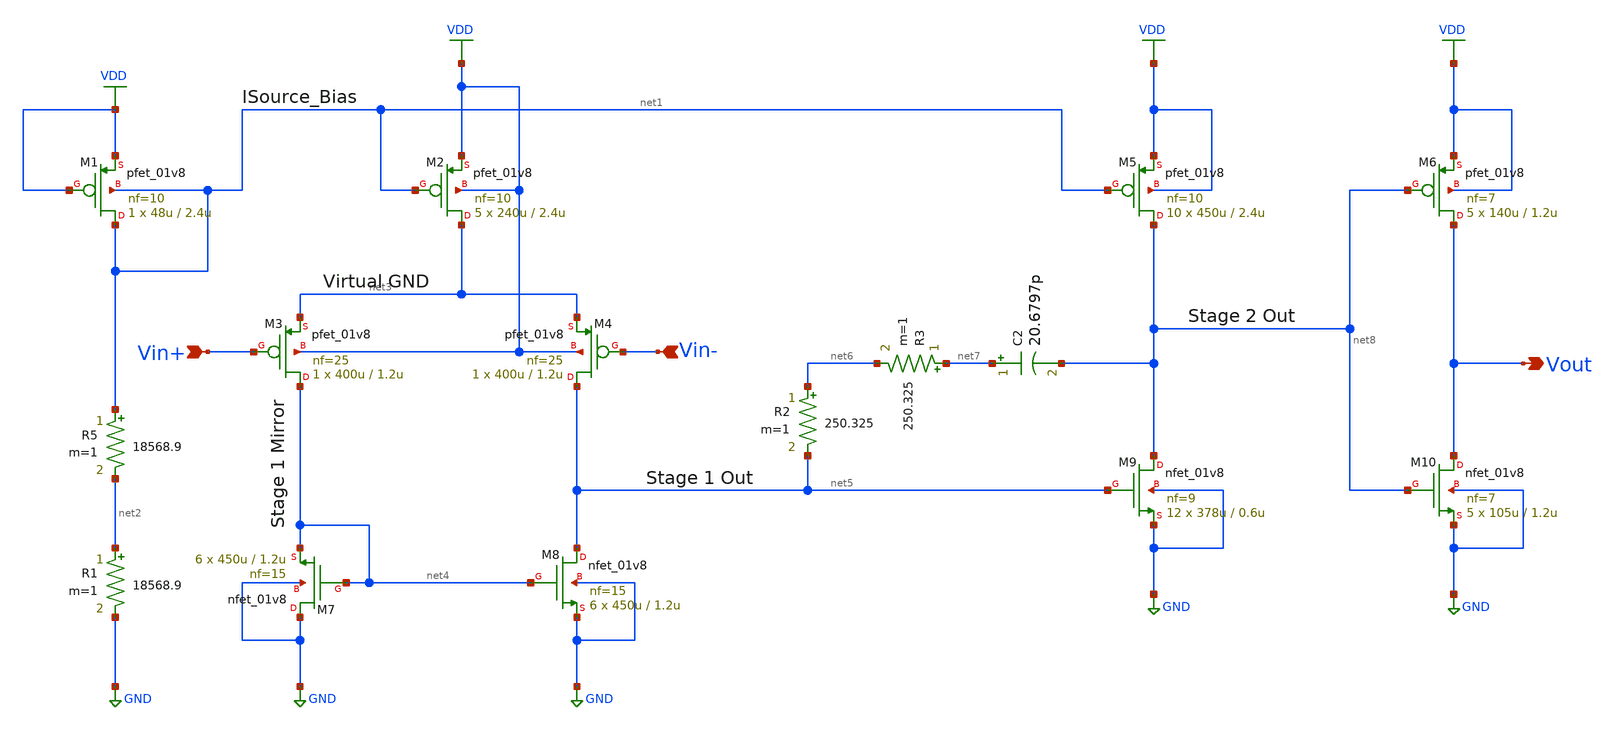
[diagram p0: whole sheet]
** sch_path: op-amp/op-amp_ver_test.sch
**.subckt op-amp_ver_test Vin+ Vin- Vout
*.ipin Vin+
*.ipin Vin-
*.opin Vout
XM1 net1 VDD VDD net1 sky130_fd_pr__pfet_01v8 L=2.4u W=48u nf=10 ad='int((nf+1)/2) * W/nf * 0.29' as='int((nf+2)/2) * W/nf * 0.29'
+ pd='2*int((nf+1)/2) * (W/nf + 0.29)' ps='2*int((nf+2)/2) * (W/nf + 0.29)' nrd='0.29 / W' nrs='0.29 / W'
+ sa=0 sb=0 sd=0 mult=1 m=1
XM2 net3 net1 VDD VDD sky130_fd_pr__pfet_01v8 L=2.4u W=240u nf=10 ad='int((nf+1)/2) * W/nf * 0.29' as='int((nf+2)/2) * W/nf * 0.29'
+ pd='2*int((nf+1)/2) * (W/nf + 0.29)' ps='2*int((nf+2)/2) * (W/nf + 0.29)' nrd='0.29 / W' nrs='0.29 / W'
+ sa=0 sb=0 sd=0 mult=5 m=5
XM3 net4 Vin+ net3 VDD sky130_fd_pr__pfet_01v8 L=1.2u W=400u nf=25 ad='int((nf+1)/2) * W/nf * 0.29' as='int((nf+2)/2) * W/nf * 0.29'
+ pd='2*int((nf+1)/2) * (W/nf + 0.29)' ps='2*int((nf+2)/2) * (W/nf + 0.29)' nrd='0.29 / W' nrs='0.29 / W'
+ sa=0 sb=0 sd=0 mult=1 m=1
XM4 net5 Vin- net3 VDD sky130_fd_pr__pfet_01v8 L=1.2u W=400u nf=25 ad='int((nf+1)/2) * W/nf * 0.29' as='int((nf+2)/2) * W/nf * 0.29'
+ pd='2*int((nf+1)/2) * (W/nf + 0.29)' ps='2*int((nf+2)/2) * (W/nf + 0.29)' nrd='0.29 / W' nrs='0.29 / W'
+ sa=0 sb=0 sd=0 mult=1 m=1
XM5 net8 net1 VDD VDD sky130_fd_pr__pfet_01v8 L=2.4u W=450u nf=10 ad='int((nf+1)/2) * W/nf * 0.29' as='int((nf+2)/2) * W/nf * 0.29'
+ pd='2*int((nf+1)/2) * (W/nf + 0.29)' ps='2*int((nf+2)/2) * (W/nf + 0.29)' nrd='0.29 / W' nrs='0.29 / W'
+ sa=0 sb=0 sd=0 mult=10 m=10
XM6 Vout net8 VDD VDD sky130_fd_pr__pfet_01v8 L=1.2u W=140u nf=7 ad='int((nf+1)/2) * W/nf * 0.29' as='int((nf+2)/2) * W/nf * 0.29'
+ pd='2*int((nf+1)/2) * (W/nf + 0.29)' ps='2*int((nf+2)/2) * (W/nf + 0.29)' nrd='0.29 / W' nrs='0.29 / W'
+ sa=0 sb=0 sd=0 mult=5 m=5
XM7 GND net4 net4 GND sky130_fd_pr__nfet_01v8 L=1.2u W=450u nf=15 ad='int((nf+1)/2) * W/nf * 0.29' as='int((nf+2)/2) * W/nf * 0.29'
+ pd='2*int((nf+1)/2) * (W/nf + 0.29)' ps='2*int((nf+2)/2) * (W/nf + 0.29)' nrd='0.29 / W' nrs='0.29 / W'
+ sa=0 sb=0 sd=0 mult=6 m=6
XM8 net5 net4 GND GND sky130_fd_pr__nfet_01v8 L=1.2u W=450u nf=15 ad='int((nf+1)/2) * W/nf * 0.29' as='int((nf+2)/2) * W/nf * 0.29'
+ pd='2*int((nf+1)/2) * (W/nf + 0.29)' ps='2*int((nf+2)/2) * (W/nf + 0.29)' nrd='0.29 / W' nrs='0.29 / W'
+ sa=0 sb=0 sd=0 mult=6 m=6
XM9 net8 net5 GND GND sky130_fd_pr__nfet_01v8 L=0.6u W=378u nf=9 ad='int((nf+1)/2) * W/nf * 0.29' as='int((nf+2)/2) * W/nf * 0.29'
+ pd='2*int((nf+1)/2) * (W/nf + 0.29)' ps='2*int((nf+2)/2) * (W/nf + 0.29)' nrd='0.29 / W' nrs='0.29 / W'
+ sa=0 sb=0 sd=0 mult=12 m=12
XM10 Vout net8 GND GND sky130_fd_pr__nfet_01v8 L=1.2u W=105u nf=7 ad='int((nf+1)/2) * W/nf * 0.29' as='int((nf+2)/2) * W/nf * 0.29'
+ pd='2*int((nf+1)/2) * (W/nf + 0.29)' ps='2*int((nf+2)/2) * (W/nf + 0.29)' nrd='0.29 / W' nrs='0.29 / W'
+ sa=0 sb=0 sd=0 mult=5 m=5
R5 net1 net2 18568.9 m=1
R1 net2 GND 18568.9 m=1
R2 net6 net5 250.325 m=1
C2 net7 net8 20.6797p m=1
R3 net7 net6 250.325 m=1
**.ends
.GLOBAL VDD
.GLOBAL GND
.end
